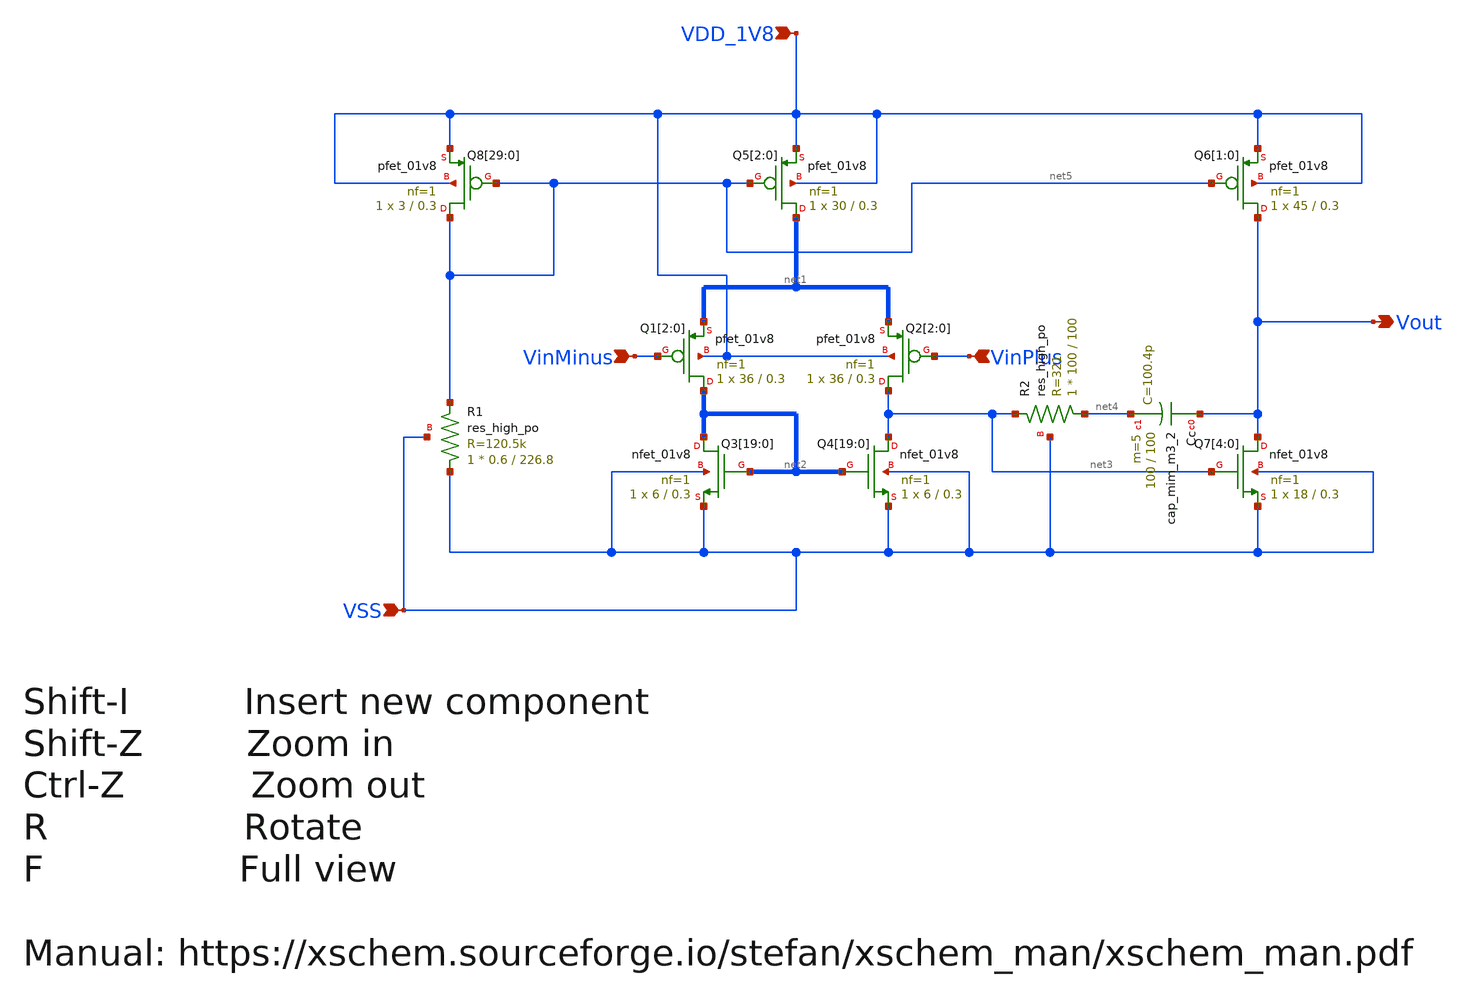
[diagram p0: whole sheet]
** sch_path: rply_mainopamp_sky130nm/design/RPLY_MAINOPAMP_SKY130NM/RPLY_MAINOPAMP.sch
**.subckt RPLY_MAINOPAMP Vout VinMinus VinPlus VDD_1V8 VSS
*.opin Vout
*.ipin VinMinus
*.ipin VinPlus
*.ipin VDD_1V8
*.ipin VSS
XQ8[29] net5 net5 VDD_1V8 VDD_1V8 sky130_fd_pr__pfet_01v8 L=0.3 W=3 nf=1 ad='int((nf+1)/2) * W/nf * 0.29'
+ as='int((nf+2)/2) * W/nf * 0.29' pd='2*int((nf+1)/2) * (W/nf + 0.29)' ps='2*int((nf+2)/2) * (W/nf + 0.29)'
+ nrd='0.29 / W' nrs='0.29 / W' sa=0 sb=0 sd=0 mult=1 m=1
XQ8[28] net5 net5 VDD_1V8 VDD_1V8 sky130_fd_pr__pfet_01v8 L=0.3 W=3 nf=1 ad='int((nf+1)/2) * W/nf * 0.29'
+ as='int((nf+2)/2) * W/nf * 0.29' pd='2*int((nf+1)/2) * (W/nf + 0.29)' ps='2*int((nf+2)/2) * (W/nf + 0.29)'
+ nrd='0.29 / W' nrs='0.29 / W' sa=0 sb=0 sd=0 mult=1 m=1
XQ8[27] net5 net5 VDD_1V8 VDD_1V8 sky130_fd_pr__pfet_01v8 L=0.3 W=3 nf=1 ad='int((nf+1)/2) * W/nf * 0.29'
+ as='int((nf+2)/2) * W/nf * 0.29' pd='2*int((nf+1)/2) * (W/nf + 0.29)' ps='2*int((nf+2)/2) * (W/nf + 0.29)'
+ nrd='0.29 / W' nrs='0.29 / W' sa=0 sb=0 sd=0 mult=1 m=1
XQ8[26] net5 net5 VDD_1V8 VDD_1V8 sky130_fd_pr__pfet_01v8 L=0.3 W=3 nf=1 ad='int((nf+1)/2) * W/nf * 0.29'
+ as='int((nf+2)/2) * W/nf * 0.29' pd='2*int((nf+1)/2) * (W/nf + 0.29)' ps='2*int((nf+2)/2) * (W/nf + 0.29)'
+ nrd='0.29 / W' nrs='0.29 / W' sa=0 sb=0 sd=0 mult=1 m=1
XQ8[25] net5 net5 VDD_1V8 VDD_1V8 sky130_fd_pr__pfet_01v8 L=0.3 W=3 nf=1 ad='int((nf+1)/2) * W/nf * 0.29'
+ as='int((nf+2)/2) * W/nf * 0.29' pd='2*int((nf+1)/2) * (W/nf + 0.29)' ps='2*int((nf+2)/2) * (W/nf + 0.29)'
+ nrd='0.29 / W' nrs='0.29 / W' sa=0 sb=0 sd=0 mult=1 m=1
XQ8[24] net5 net5 VDD_1V8 VDD_1V8 sky130_fd_pr__pfet_01v8 L=0.3 W=3 nf=1 ad='int((nf+1)/2) * W/nf * 0.29'
+ as='int((nf+2)/2) * W/nf * 0.29' pd='2*int((nf+1)/2) * (W/nf + 0.29)' ps='2*int((nf+2)/2) * (W/nf + 0.29)'
+ nrd='0.29 / W' nrs='0.29 / W' sa=0 sb=0 sd=0 mult=1 m=1
XQ8[23] net5 net5 VDD_1V8 VDD_1V8 sky130_fd_pr__pfet_01v8 L=0.3 W=3 nf=1 ad='int((nf+1)/2) * W/nf * 0.29'
+ as='int((nf+2)/2) * W/nf * 0.29' pd='2*int((nf+1)/2) * (W/nf + 0.29)' ps='2*int((nf+2)/2) * (W/nf + 0.29)'
+ nrd='0.29 / W' nrs='0.29 / W' sa=0 sb=0 sd=0 mult=1 m=1
XQ8[22] net5 net5 VDD_1V8 VDD_1V8 sky130_fd_pr__pfet_01v8 L=0.3 W=3 nf=1 ad='int((nf+1)/2) * W/nf * 0.29'
+ as='int((nf+2)/2) * W/nf * 0.29' pd='2*int((nf+1)/2) * (W/nf + 0.29)' ps='2*int((nf+2)/2) * (W/nf + 0.29)'
+ nrd='0.29 / W' nrs='0.29 / W' sa=0 sb=0 sd=0 mult=1 m=1
XQ8[21] net5 net5 VDD_1V8 VDD_1V8 sky130_fd_pr__pfet_01v8 L=0.3 W=3 nf=1 ad='int((nf+1)/2) * W/nf * 0.29'
+ as='int((nf+2)/2) * W/nf * 0.29' pd='2*int((nf+1)/2) * (W/nf + 0.29)' ps='2*int((nf+2)/2) * (W/nf + 0.29)'
+ nrd='0.29 / W' nrs='0.29 / W' sa=0 sb=0 sd=0 mult=1 m=1
XQ8[20] net5 net5 VDD_1V8 VDD_1V8 sky130_fd_pr__pfet_01v8 L=0.3 W=3 nf=1 ad='int((nf+1)/2) * W/nf * 0.29'
+ as='int((nf+2)/2) * W/nf * 0.29' pd='2*int((nf+1)/2) * (W/nf + 0.29)' ps='2*int((nf+2)/2) * (W/nf + 0.29)'
+ nrd='0.29 / W' nrs='0.29 / W' sa=0 sb=0 sd=0 mult=1 m=1
XQ8[19] net5 net5 VDD_1V8 VDD_1V8 sky130_fd_pr__pfet_01v8 L=0.3 W=3 nf=1 ad='int((nf+1)/2) * W/nf * 0.29'
+ as='int((nf+2)/2) * W/nf * 0.29' pd='2*int((nf+1)/2) * (W/nf + 0.29)' ps='2*int((nf+2)/2) * (W/nf + 0.29)'
+ nrd='0.29 / W' nrs='0.29 / W' sa=0 sb=0 sd=0 mult=1 m=1
XQ8[18] net5 net5 VDD_1V8 VDD_1V8 sky130_fd_pr__pfet_01v8 L=0.3 W=3 nf=1 ad='int((nf+1)/2) * W/nf * 0.29'
+ as='int((nf+2)/2) * W/nf * 0.29' pd='2*int((nf+1)/2) * (W/nf + 0.29)' ps='2*int((nf+2)/2) * (W/nf + 0.29)'
+ nrd='0.29 / W' nrs='0.29 / W' sa=0 sb=0 sd=0 mult=1 m=1
XQ8[17] net5 net5 VDD_1V8 VDD_1V8 sky130_fd_pr__pfet_01v8 L=0.3 W=3 nf=1 ad='int((nf+1)/2) * W/nf * 0.29'
+ as='int((nf+2)/2) * W/nf * 0.29' pd='2*int((nf+1)/2) * (W/nf + 0.29)' ps='2*int((nf+2)/2) * (W/nf + 0.29)'
+ nrd='0.29 / W' nrs='0.29 / W' sa=0 sb=0 sd=0 mult=1 m=1
XQ8[16] net5 net5 VDD_1V8 VDD_1V8 sky130_fd_pr__pfet_01v8 L=0.3 W=3 nf=1 ad='int((nf+1)/2) * W/nf * 0.29'
+ as='int((nf+2)/2) * W/nf * 0.29' pd='2*int((nf+1)/2) * (W/nf + 0.29)' ps='2*int((nf+2)/2) * (W/nf + 0.29)'
+ nrd='0.29 / W' nrs='0.29 / W' sa=0 sb=0 sd=0 mult=1 m=1
XQ8[15] net5 net5 VDD_1V8 VDD_1V8 sky130_fd_pr__pfet_01v8 L=0.3 W=3 nf=1 ad='int((nf+1)/2) * W/nf * 0.29'
+ as='int((nf+2)/2) * W/nf * 0.29' pd='2*int((nf+1)/2) * (W/nf + 0.29)' ps='2*int((nf+2)/2) * (W/nf + 0.29)'
+ nrd='0.29 / W' nrs='0.29 / W' sa=0 sb=0 sd=0 mult=1 m=1
XQ8[14] net5 net5 VDD_1V8 VDD_1V8 sky130_fd_pr__pfet_01v8 L=0.3 W=3 nf=1 ad='int((nf+1)/2) * W/nf * 0.29'
+ as='int((nf+2)/2) * W/nf * 0.29' pd='2*int((nf+1)/2) * (W/nf + 0.29)' ps='2*int((nf+2)/2) * (W/nf + 0.29)'
+ nrd='0.29 / W' nrs='0.29 / W' sa=0 sb=0 sd=0 mult=1 m=1
XQ8[13] net5 net5 VDD_1V8 VDD_1V8 sky130_fd_pr__pfet_01v8 L=0.3 W=3 nf=1 ad='int((nf+1)/2) * W/nf * 0.29'
+ as='int((nf+2)/2) * W/nf * 0.29' pd='2*int((nf+1)/2) * (W/nf + 0.29)' ps='2*int((nf+2)/2) * (W/nf + 0.29)'
+ nrd='0.29 / W' nrs='0.29 / W' sa=0 sb=0 sd=0 mult=1 m=1
XQ8[12] net5 net5 VDD_1V8 VDD_1V8 sky130_fd_pr__pfet_01v8 L=0.3 W=3 nf=1 ad='int((nf+1)/2) * W/nf * 0.29'
+ as='int((nf+2)/2) * W/nf * 0.29' pd='2*int((nf+1)/2) * (W/nf + 0.29)' ps='2*int((nf+2)/2) * (W/nf + 0.29)'
+ nrd='0.29 / W' nrs='0.29 / W' sa=0 sb=0 sd=0 mult=1 m=1
XQ8[11] net5 net5 VDD_1V8 VDD_1V8 sky130_fd_pr__pfet_01v8 L=0.3 W=3 nf=1 ad='int((nf+1)/2) * W/nf * 0.29'
+ as='int((nf+2)/2) * W/nf * 0.29' pd='2*int((nf+1)/2) * (W/nf + 0.29)' ps='2*int((nf+2)/2) * (W/nf + 0.29)'
+ nrd='0.29 / W' nrs='0.29 / W' sa=0 sb=0 sd=0 mult=1 m=1
XQ8[10] net5 net5 VDD_1V8 VDD_1V8 sky130_fd_pr__pfet_01v8 L=0.3 W=3 nf=1 ad='int((nf+1)/2) * W/nf * 0.29'
+ as='int((nf+2)/2) * W/nf * 0.29' pd='2*int((nf+1)/2) * (W/nf + 0.29)' ps='2*int((nf+2)/2) * (W/nf + 0.29)'
+ nrd='0.29 / W' nrs='0.29 / W' sa=0 sb=0 sd=0 mult=1 m=1
XQ8[9] net5 net5 VDD_1V8 VDD_1V8 sky130_fd_pr__pfet_01v8 L=0.3 W=3 nf=1 ad='int((nf+1)/2) * W/nf * 0.29'
+ as='int((nf+2)/2) * W/nf * 0.29' pd='2*int((nf+1)/2) * (W/nf + 0.29)' ps='2*int((nf+2)/2) * (W/nf + 0.29)'
+ nrd='0.29 / W' nrs='0.29 / W' sa=0 sb=0 sd=0 mult=1 m=1
XQ8[8] net5 net5 VDD_1V8 VDD_1V8 sky130_fd_pr__pfet_01v8 L=0.3 W=3 nf=1 ad='int((nf+1)/2) * W/nf * 0.29'
+ as='int((nf+2)/2) * W/nf * 0.29' pd='2*int((nf+1)/2) * (W/nf + 0.29)' ps='2*int((nf+2)/2) * (W/nf + 0.29)'
+ nrd='0.29 / W' nrs='0.29 / W' sa=0 sb=0 sd=0 mult=1 m=1
XQ8[7] net5 net5 VDD_1V8 VDD_1V8 sky130_fd_pr__pfet_01v8 L=0.3 W=3 nf=1 ad='int((nf+1)/2) * W/nf * 0.29'
+ as='int((nf+2)/2) * W/nf * 0.29' pd='2*int((nf+1)/2) * (W/nf + 0.29)' ps='2*int((nf+2)/2) * (W/nf + 0.29)'
+ nrd='0.29 / W' nrs='0.29 / W' sa=0 sb=0 sd=0 mult=1 m=1
XQ8[6] net5 net5 VDD_1V8 VDD_1V8 sky130_fd_pr__pfet_01v8 L=0.3 W=3 nf=1 ad='int((nf+1)/2) * W/nf * 0.29'
+ as='int((nf+2)/2) * W/nf * 0.29' pd='2*int((nf+1)/2) * (W/nf + 0.29)' ps='2*int((nf+2)/2) * (W/nf + 0.29)'
+ nrd='0.29 / W' nrs='0.29 / W' sa=0 sb=0 sd=0 mult=1 m=1
XQ8[5] net5 net5 VDD_1V8 VDD_1V8 sky130_fd_pr__pfet_01v8 L=0.3 W=3 nf=1 ad='int((nf+1)/2) * W/nf * 0.29'
+ as='int((nf+2)/2) * W/nf * 0.29' pd='2*int((nf+1)/2) * (W/nf + 0.29)' ps='2*int((nf+2)/2) * (W/nf + 0.29)'
+ nrd='0.29 / W' nrs='0.29 / W' sa=0 sb=0 sd=0 mult=1 m=1
XQ8[4] net5 net5 VDD_1V8 VDD_1V8 sky130_fd_pr__pfet_01v8 L=0.3 W=3 nf=1 ad='int((nf+1)/2) * W/nf * 0.29'
+ as='int((nf+2)/2) * W/nf * 0.29' pd='2*int((nf+1)/2) * (W/nf + 0.29)' ps='2*int((nf+2)/2) * (W/nf + 0.29)'
+ nrd='0.29 / W' nrs='0.29 / W' sa=0 sb=0 sd=0 mult=1 m=1
XQ8[3] net5 net5 VDD_1V8 VDD_1V8 sky130_fd_pr__pfet_01v8 L=0.3 W=3 nf=1 ad='int((nf+1)/2) * W/nf * 0.29'
+ as='int((nf+2)/2) * W/nf * 0.29' pd='2*int((nf+1)/2) * (W/nf + 0.29)' ps='2*int((nf+2)/2) * (W/nf + 0.29)'
+ nrd='0.29 / W' nrs='0.29 / W' sa=0 sb=0 sd=0 mult=1 m=1
XQ8[2] net5 net5 VDD_1V8 VDD_1V8 sky130_fd_pr__pfet_01v8 L=0.3 W=3 nf=1 ad='int((nf+1)/2) * W/nf * 0.29'
+ as='int((nf+2)/2) * W/nf * 0.29' pd='2*int((nf+1)/2) * (W/nf + 0.29)' ps='2*int((nf+2)/2) * (W/nf + 0.29)'
+ nrd='0.29 / W' nrs='0.29 / W' sa=0 sb=0 sd=0 mult=1 m=1
XQ8[1] net5 net5 VDD_1V8 VDD_1V8 sky130_fd_pr__pfet_01v8 L=0.3 W=3 nf=1 ad='int((nf+1)/2) * W/nf * 0.29'
+ as='int((nf+2)/2) * W/nf * 0.29' pd='2*int((nf+1)/2) * (W/nf + 0.29)' ps='2*int((nf+2)/2) * (W/nf + 0.29)'
+ nrd='0.29 / W' nrs='0.29 / W' sa=0 sb=0 sd=0 mult=1 m=1
XQ8[0] net5 net5 VDD_1V8 VDD_1V8 sky130_fd_pr__pfet_01v8 L=0.3 W=3 nf=1 ad='int((nf+1)/2) * W/nf * 0.29'
+ as='int((nf+2)/2) * W/nf * 0.29' pd='2*int((nf+1)/2) * (W/nf + 0.29)' ps='2*int((nf+2)/2) * (W/nf + 0.29)'
+ nrd='0.29 / W' nrs='0.29 / W' sa=0 sb=0 sd=0 mult=1 m=1
XQ5[2] net1[2] net5 VDD_1V8 VDD_1V8 sky130_fd_pr__pfet_01v8 L=0.3 W=30 nf=1 ad='int((nf+1)/2) * W/nf * 0.29'
+ as='int((nf+2)/2) * W/nf * 0.29' pd='2*int((nf+1)/2) * (W/nf + 0.29)' ps='2*int((nf+2)/2) * (W/nf + 0.29)'
+ nrd='0.29 / W' nrs='0.29 / W' sa=0 sb=0 sd=0 mult=1 m=1
XQ5[1] net1[1] net5 VDD_1V8 VDD_1V8 sky130_fd_pr__pfet_01v8 L=0.3 W=30 nf=1 ad='int((nf+1)/2) * W/nf * 0.29'
+ as='int((nf+2)/2) * W/nf * 0.29' pd='2*int((nf+1)/2) * (W/nf + 0.29)' ps='2*int((nf+2)/2) * (W/nf + 0.29)'
+ nrd='0.29 / W' nrs='0.29 / W' sa=0 sb=0 sd=0 mult=1 m=1
XQ5[0] net1[0] net5 VDD_1V8 VDD_1V8 sky130_fd_pr__pfet_01v8 L=0.3 W=30 nf=1 ad='int((nf+1)/2) * W/nf * 0.29'
+ as='int((nf+2)/2) * W/nf * 0.29' pd='2*int((nf+1)/2) * (W/nf + 0.29)' ps='2*int((nf+2)/2) * (W/nf + 0.29)'
+ nrd='0.29 / W' nrs='0.29 / W' sa=0 sb=0 sd=0 mult=1 m=1
XQ6[1] Vout net5 VDD_1V8 VDD_1V8 sky130_fd_pr__pfet_01v8 L=0.3 W=45 nf=1 ad='int((nf+1)/2) * W/nf * 0.29'
+ as='int((nf+2)/2) * W/nf * 0.29' pd='2*int((nf+1)/2) * (W/nf + 0.29)' ps='2*int((nf+2)/2) * (W/nf + 0.29)'
+ nrd='0.29 / W' nrs='0.29 / W' sa=0 sb=0 sd=0 mult=1 m=1
XQ6[0] Vout net5 VDD_1V8 VDD_1V8 sky130_fd_pr__pfet_01v8 L=0.3 W=45 nf=1 ad='int((nf+1)/2) * W/nf * 0.29'
+ as='int((nf+2)/2) * W/nf * 0.29' pd='2*int((nf+1)/2) * (W/nf + 0.29)' ps='2*int((nf+2)/2) * (W/nf + 0.29)'
+ nrd='0.29 / W' nrs='0.29 / W' sa=0 sb=0 sd=0 mult=1 m=1
XQ1[2] net2[2] VinMinus net1[2] VDD_1V8 sky130_fd_pr__pfet_01v8 L=0.3 W=36 nf=1 ad='int((nf+1)/2) * W/nf * 0.29'
+ as='int((nf+2)/2) * W/nf * 0.29' pd='2*int((nf+1)/2) * (W/nf + 0.29)' ps='2*int((nf+2)/2) * (W/nf + 0.29)'
+ nrd='0.29 / W' nrs='0.29 / W' sa=0 sb=0 sd=0 mult=1 m=1
XQ1[1] net2[1] VinMinus net1[1] VDD_1V8 sky130_fd_pr__pfet_01v8 L=0.3 W=36 nf=1 ad='int((nf+1)/2) * W/nf * 0.29'
+ as='int((nf+2)/2) * W/nf * 0.29' pd='2*int((nf+1)/2) * (W/nf + 0.29)' ps='2*int((nf+2)/2) * (W/nf + 0.29)'
+ nrd='0.29 / W' nrs='0.29 / W' sa=0 sb=0 sd=0 mult=1 m=1
XQ1[0] net2[0] VinMinus net1[0] VDD_1V8 sky130_fd_pr__pfet_01v8 L=0.3 W=36 nf=1 ad='int((nf+1)/2) * W/nf * 0.29'
+ as='int((nf+2)/2) * W/nf * 0.29' pd='2*int((nf+1)/2) * (W/nf + 0.29)' ps='2*int((nf+2)/2) * (W/nf + 0.29)'
+ nrd='0.29 / W' nrs='0.29 / W' sa=0 sb=0 sd=0 mult=1 m=1
XQ2[2] net3 VinPlus net1[2] VDD_1V8 sky130_fd_pr__pfet_01v8 L=0.3 W=36 nf=1 ad='int((nf+1)/2) * W/nf * 0.29'
+ as='int((nf+2)/2) * W/nf * 0.29' pd='2*int((nf+1)/2) * (W/nf + 0.29)' ps='2*int((nf+2)/2) * (W/nf + 0.29)'
+ nrd='0.29 / W' nrs='0.29 / W' sa=0 sb=0 sd=0 mult=1 m=1
XQ2[1] net3 VinPlus net1[1] VDD_1V8 sky130_fd_pr__pfet_01v8 L=0.3 W=36 nf=1 ad='int((nf+1)/2) * W/nf * 0.29'
+ as='int((nf+2)/2) * W/nf * 0.29' pd='2*int((nf+1)/2) * (W/nf + 0.29)' ps='2*int((nf+2)/2) * (W/nf + 0.29)'
+ nrd='0.29 / W' nrs='0.29 / W' sa=0 sb=0 sd=0 mult=1 m=1
XQ2[0] net3 VinPlus net1[0] VDD_1V8 sky130_fd_pr__pfet_01v8 L=0.3 W=36 nf=1 ad='int((nf+1)/2) * W/nf * 0.29'
+ as='int((nf+2)/2) * W/nf * 0.29' pd='2*int((nf+1)/2) * (W/nf + 0.29)' ps='2*int((nf+2)/2) * (W/nf + 0.29)'
+ nrd='0.29 / W' nrs='0.29 / W' sa=0 sb=0 sd=0 mult=1 m=1
XQ4[19] net3 net2[2] VSS VSS sky130_fd_pr__nfet_01v8 L=0.3 W=6 nf=1 ad='int((nf+1)/2) * W/nf * 0.29'
+ as='int((nf+2)/2) * W/nf * 0.29' pd='2*int((nf+1)/2) * (W/nf + 0.29)' ps='2*int((nf+2)/2) * (W/nf + 0.29)'
+ nrd='0.29 / W' nrs='0.29 / W' sa=0 sb=0 sd=0 mult=1 m=1
XQ4[18] net3 net2[1] VSS VSS sky130_fd_pr__nfet_01v8 L=0.3 W=6 nf=1 ad='int((nf+1)/2) * W/nf * 0.29'
+ as='int((nf+2)/2) * W/nf * 0.29' pd='2*int((nf+1)/2) * (W/nf + 0.29)' ps='2*int((nf+2)/2) * (W/nf + 0.29)'
+ nrd='0.29 / W' nrs='0.29 / W' sa=0 sb=0 sd=0 mult=1 m=1
XQ4[17] net3 net2[0] VSS VSS sky130_fd_pr__nfet_01v8 L=0.3 W=6 nf=1 ad='int((nf+1)/2) * W/nf * 0.29'
+ as='int((nf+2)/2) * W/nf * 0.29' pd='2*int((nf+1)/2) * (W/nf + 0.29)' ps='2*int((nf+2)/2) * (W/nf + 0.29)'
+ nrd='0.29 / W' nrs='0.29 / W' sa=0 sb=0 sd=0 mult=1 m=1
XQ4[16] net3 net2[2] VSS VSS sky130_fd_pr__nfet_01v8 L=0.3 W=6 nf=1 ad='int((nf+1)/2) * W/nf * 0.29'
+ as='int((nf+2)/2) * W/nf * 0.29' pd='2*int((nf+1)/2) * (W/nf + 0.29)' ps='2*int((nf+2)/2) * (W/nf + 0.29)'
+ nrd='0.29 / W' nrs='0.29 / W' sa=0 sb=0 sd=0 mult=1 m=1
XQ4[15] net3 net2[1] VSS VSS sky130_fd_pr__nfet_01v8 L=0.3 W=6 nf=1 ad='int((nf+1)/2) * W/nf * 0.29'
+ as='int((nf+2)/2) * W/nf * 0.29' pd='2*int((nf+1)/2) * (W/nf + 0.29)' ps='2*int((nf+2)/2) * (W/nf + 0.29)'
+ nrd='0.29 / W' nrs='0.29 / W' sa=0 sb=0 sd=0 mult=1 m=1
XQ4[14] net3 net2[0] VSS VSS sky130_fd_pr__nfet_01v8 L=0.3 W=6 nf=1 ad='int((nf+1)/2) * W/nf * 0.29'
+ as='int((nf+2)/2) * W/nf * 0.29' pd='2*int((nf+1)/2) * (W/nf + 0.29)' ps='2*int((nf+2)/2) * (W/nf + 0.29)'
+ nrd='0.29 / W' nrs='0.29 / W' sa=0 sb=0 sd=0 mult=1 m=1
XQ4[13] net3 net2[2] VSS VSS sky130_fd_pr__nfet_01v8 L=0.3 W=6 nf=1 ad='int((nf+1)/2) * W/nf * 0.29'
+ as='int((nf+2)/2) * W/nf * 0.29' pd='2*int((nf+1)/2) * (W/nf + 0.29)' ps='2*int((nf+2)/2) * (W/nf + 0.29)'
+ nrd='0.29 / W' nrs='0.29 / W' sa=0 sb=0 sd=0 mult=1 m=1
XQ4[12] net3 net2[1] VSS VSS sky130_fd_pr__nfet_01v8 L=0.3 W=6 nf=1 ad='int((nf+1)/2) * W/nf * 0.29'
+ as='int((nf+2)/2) * W/nf * 0.29' pd='2*int((nf+1)/2) * (W/nf + 0.29)' ps='2*int((nf+2)/2) * (W/nf + 0.29)'
+ nrd='0.29 / W' nrs='0.29 / W' sa=0 sb=0 sd=0 mult=1 m=1
XQ4[11] net3 net2[0] VSS VSS sky130_fd_pr__nfet_01v8 L=0.3 W=6 nf=1 ad='int((nf+1)/2) * W/nf * 0.29'
+ as='int((nf+2)/2) * W/nf * 0.29' pd='2*int((nf+1)/2) * (W/nf + 0.29)' ps='2*int((nf+2)/2) * (W/nf + 0.29)'
+ nrd='0.29 / W' nrs='0.29 / W' sa=0 sb=0 sd=0 mult=1 m=1
XQ4[10] net3 net2[2] VSS VSS sky130_fd_pr__nfet_01v8 L=0.3 W=6 nf=1 ad='int((nf+1)/2) * W/nf * 0.29'
+ as='int((nf+2)/2) * W/nf * 0.29' pd='2*int((nf+1)/2) * (W/nf + 0.29)' ps='2*int((nf+2)/2) * (W/nf + 0.29)'
+ nrd='0.29 / W' nrs='0.29 / W' sa=0 sb=0 sd=0 mult=1 m=1
XQ4[9] net3 net2[1] VSS VSS sky130_fd_pr__nfet_01v8 L=0.3 W=6 nf=1 ad='int((nf+1)/2) * W/nf * 0.29' as='int((nf+2)/2) * W/nf * 0.29'
+ pd='2*int((nf+1)/2) * (W/nf + 0.29)' ps='2*int((nf+2)/2) * (W/nf + 0.29)' nrd='0.29 / W' nrs='0.29 / W'
+ sa=0 sb=0 sd=0 mult=1 m=1
XQ4[8] net3 net2[0] VSS VSS sky130_fd_pr__nfet_01v8 L=0.3 W=6 nf=1 ad='int((nf+1)/2) * W/nf * 0.29' as='int((nf+2)/2) * W/nf * 0.29'
+ pd='2*int((nf+1)/2) * (W/nf + 0.29)' ps='2*int((nf+2)/2) * (W/nf + 0.29)' nrd='0.29 / W' nrs='0.29 / W'
+ sa=0 sb=0 sd=0 mult=1 m=1
XQ4[7] net3 net2[2] VSS VSS sky130_fd_pr__nfet_01v8 L=0.3 W=6 nf=1 ad='int((nf+1)/2) * W/nf * 0.29' as='int((nf+2)/2) * W/nf * 0.29'
+ pd='2*int((nf+1)/2) * (W/nf + 0.29)' ps='2*int((nf+2)/2) * (W/nf + 0.29)' nrd='0.29 / W' nrs='0.29 / W'
+ sa=0 sb=0 sd=0 mult=1 m=1
XQ4[6] net3 net2[1] VSS VSS sky130_fd_pr__nfet_01v8 L=0.3 W=6 nf=1 ad='int((nf+1)/2) * W/nf * 0.29' as='int((nf+2)/2) * W/nf * 0.29'
+ pd='2*int((nf+1)/2) * (W/nf + 0.29)' ps='2*int((nf+2)/2) * (W/nf + 0.29)' nrd='0.29 / W' nrs='0.29 / W'
+ sa=0 sb=0 sd=0 mult=1 m=1
XQ4[5] net3 net2[0] VSS VSS sky130_fd_pr__nfet_01v8 L=0.3 W=6 nf=1 ad='int((nf+1)/2) * W/nf * 0.29' as='int((nf+2)/2) * W/nf * 0.29'
+ pd='2*int((nf+1)/2) * (W/nf + 0.29)' ps='2*int((nf+2)/2) * (W/nf + 0.29)' nrd='0.29 / W' nrs='0.29 / W'
+ sa=0 sb=0 sd=0 mult=1 m=1
XQ4[4] net3 net2[2] VSS VSS sky130_fd_pr__nfet_01v8 L=0.3 W=6 nf=1 ad='int((nf+1)/2) * W/nf * 0.29' as='int((nf+2)/2) * W/nf * 0.29'
+ pd='2*int((nf+1)/2) * (W/nf + 0.29)' ps='2*int((nf+2)/2) * (W/nf + 0.29)' nrd='0.29 / W' nrs='0.29 / W'
+ sa=0 sb=0 sd=0 mult=1 m=1
XQ4[3] net3 net2[1] VSS VSS sky130_fd_pr__nfet_01v8 L=0.3 W=6 nf=1 ad='int((nf+1)/2) * W/nf * 0.29' as='int((nf+2)/2) * W/nf * 0.29'
+ pd='2*int((nf+1)/2) * (W/nf + 0.29)' ps='2*int((nf+2)/2) * (W/nf + 0.29)' nrd='0.29 / W' nrs='0.29 / W'
+ sa=0 sb=0 sd=0 mult=1 m=1
XQ4[2] net3 net2[0] VSS VSS sky130_fd_pr__nfet_01v8 L=0.3 W=6 nf=1 ad='int((nf+1)/2) * W/nf * 0.29' as='int((nf+2)/2) * W/nf * 0.29'
+ pd='2*int((nf+1)/2) * (W/nf + 0.29)' ps='2*int((nf+2)/2) * (W/nf + 0.29)' nrd='0.29 / W' nrs='0.29 / W'
+ sa=0 sb=0 sd=0 mult=1 m=1
XQ4[1] net3 net2[2] VSS VSS sky130_fd_pr__nfet_01v8 L=0.3 W=6 nf=1 ad='int((nf+1)/2) * W/nf * 0.29' as='int((nf+2)/2) * W/nf * 0.29'
+ pd='2*int((nf+1)/2) * (W/nf + 0.29)' ps='2*int((nf+2)/2) * (W/nf + 0.29)' nrd='0.29 / W' nrs='0.29 / W'
+ sa=0 sb=0 sd=0 mult=1 m=1
XQ4[0] net3 net2[1] VSS VSS sky130_fd_pr__nfet_01v8 L=0.3 W=6 nf=1 ad='int((nf+1)/2) * W/nf * 0.29' as='int((nf+2)/2) * W/nf * 0.29'
+ pd='2*int((nf+1)/2) * (W/nf + 0.29)' ps='2*int((nf+2)/2) * (W/nf + 0.29)' nrd='0.29 / W' nrs='0.29 / W'
+ sa=0 sb=0 sd=0 mult=1 m=1
XQ3[19] net2[2] net2[2] VSS VSS sky130_fd_pr__nfet_01v8 L=0.3 W=6 nf=1 ad='int((nf+1)/2) * W/nf * 0.29'
+ as='int((nf+2)/2) * W/nf * 0.29' pd='2*int((nf+1)/2) * (W/nf + 0.29)' ps='2*int((nf+2)/2) * (W/nf + 0.29)'
+ nrd='0.29 / W' nrs='0.29 / W' sa=0 sb=0 sd=0 mult=1 m=1
XQ3[18] net2[1] net2[1] VSS VSS sky130_fd_pr__nfet_01v8 L=0.3 W=6 nf=1 ad='int((nf+1)/2) * W/nf * 0.29'
+ as='int((nf+2)/2) * W/nf * 0.29' pd='2*int((nf+1)/2) * (W/nf + 0.29)' ps='2*int((nf+2)/2) * (W/nf + 0.29)'
+ nrd='0.29 / W' nrs='0.29 / W' sa=0 sb=0 sd=0 mult=1 m=1
XQ3[17] net2[0] net2[0] VSS VSS sky130_fd_pr__nfet_01v8 L=0.3 W=6 nf=1 ad='int((nf+1)/2) * W/nf * 0.29'
+ as='int((nf+2)/2) * W/nf * 0.29' pd='2*int((nf+1)/2) * (W/nf + 0.29)' ps='2*int((nf+2)/2) * (W/nf + 0.29)'
+ nrd='0.29 / W' nrs='0.29 / W' sa=0 sb=0 sd=0 mult=1 m=1
XQ3[16] net2[2] net2[2] VSS VSS sky130_fd_pr__nfet_01v8 L=0.3 W=6 nf=1 ad='int((nf+1)/2) * W/nf * 0.29'
+ as='int((nf+2)/2) * W/nf * 0.29' pd='2*int((nf+1)/2) * (W/nf + 0.29)' ps='2*int((nf+2)/2) * (W/nf + 0.29)'
+ nrd='0.29 / W' nrs='0.29 / W' sa=0 sb=0 sd=0 mult=1 m=1
XQ3[15] net2[1] net2[1] VSS VSS sky130_fd_pr__nfet_01v8 L=0.3 W=6 nf=1 ad='int((nf+1)/2) * W/nf * 0.29'
+ as='int((nf+2)/2) * W/nf * 0.29' pd='2*int((nf+1)/2) * (W/nf + 0.29)' ps='2*int((nf+2)/2) * (W/nf + 0.29)'
+ nrd='0.29 / W' nrs='0.29 / W' sa=0 sb=0 sd=0 mult=1 m=1
XQ3[14] net2[0] net2[0] VSS VSS sky130_fd_pr__nfet_01v8 L=0.3 W=6 nf=1 ad='int((nf+1)/2) * W/nf * 0.29'
+ as='int((nf+2)/2) * W/nf * 0.29' pd='2*int((nf+1)/2) * (W/nf + 0.29)' ps='2*int((nf+2)/2) * (W/nf + 0.29)'
+ nrd='0.29 / W' nrs='0.29 / W' sa=0 sb=0 sd=0 mult=1 m=1
XQ3[13] net2[2] net2[2] VSS VSS sky130_fd_pr__nfet_01v8 L=0.3 W=6 nf=1 ad='int((nf+1)/2) * W/nf * 0.29'
+ as='int((nf+2)/2) * W/nf * 0.29' pd='2*int((nf+1)/2) * (W/nf + 0.29)' ps='2*int((nf+2)/2) * (W/nf + 0.29)'
+ nrd='0.29 / W' nrs='0.29 / W' sa=0 sb=0 sd=0 mult=1 m=1
XQ3[12] net2[1] net2[1] VSS VSS sky130_fd_pr__nfet_01v8 L=0.3 W=6 nf=1 ad='int((nf+1)/2) * W/nf * 0.29'
+ as='int((nf+2)/2) * W/nf * 0.29' pd='2*int((nf+1)/2) * (W/nf + 0.29)' ps='2*int((nf+2)/2) * (W/nf + 0.29)'
+ nrd='0.29 / W' nrs='0.29 / W' sa=0 sb=0 sd=0 mult=1 m=1
XQ3[11] net2[0] net2[0] VSS VSS sky130_fd_pr__nfet_01v8 L=0.3 W=6 nf=1 ad='int((nf+1)/2) * W/nf * 0.29'
+ as='int((nf+2)/2) * W/nf * 0.29' pd='2*int((nf+1)/2) * (W/nf + 0.29)' ps='2*int((nf+2)/2) * (W/nf + 0.29)'
+ nrd='0.29 / W' nrs='0.29 / W' sa=0 sb=0 sd=0 mult=1 m=1
XQ3[10] net2[2] net2[2] VSS VSS sky130_fd_pr__nfet_01v8 L=0.3 W=6 nf=1 ad='int((nf+1)/2) * W/nf * 0.29'
+ as='int((nf+2)/2) * W/nf * 0.29' pd='2*int((nf+1)/2) * (W/nf + 0.29)' ps='2*int((nf+2)/2) * (W/nf + 0.29)'
+ nrd='0.29 / W' nrs='0.29 / W' sa=0 sb=0 sd=0 mult=1 m=1
XQ3[9] net2[1] net2[1] VSS VSS sky130_fd_pr__nfet_01v8 L=0.3 W=6 nf=1 ad='int((nf+1)/2) * W/nf * 0.29'
+ as='int((nf+2)/2) * W/nf * 0.29' pd='2*int((nf+1)/2) * (W/nf + 0.29)' ps='2*int((nf+2)/2) * (W/nf + 0.29)'
+ nrd='0.29 / W' nrs='0.29 / W' sa=0 sb=0 sd=0 mult=1 m=1
XQ3[8] net2[0] net2[0] VSS VSS sky130_fd_pr__nfet_01v8 L=0.3 W=6 nf=1 ad='int((nf+1)/2) * W/nf * 0.29'
+ as='int((nf+2)/2) * W/nf * 0.29' pd='2*int((nf+1)/2) * (W/nf + 0.29)' ps='2*int((nf+2)/2) * (W/nf + 0.29)'
+ nrd='0.29 / W' nrs='0.29 / W' sa=0 sb=0 sd=0 mult=1 m=1
XQ3[7] net2[2] net2[2] VSS VSS sky130_fd_pr__nfet_01v8 L=0.3 W=6 nf=1 ad='int((nf+1)/2) * W/nf * 0.29'
+ as='int((nf+2)/2) * W/nf * 0.29' pd='2*int((nf+1)/2) * (W/nf + 0.29)' ps='2*int((nf+2)/2) * (W/nf + 0.29)'
+ nrd='0.29 / W' nrs='0.29 / W' sa=0 sb=0 sd=0 mult=1 m=1
XQ3[6] net2[1] net2[1] VSS VSS sky130_fd_pr__nfet_01v8 L=0.3 W=6 nf=1 ad='int((nf+1)/2) * W/nf * 0.29'
+ as='int((nf+2)/2) * W/nf * 0.29' pd='2*int((nf+1)/2) * (W/nf + 0.29)' ps='2*int((nf+2)/2) * (W/nf + 0.29)'
+ nrd='0.29 / W' nrs='0.29 / W' sa=0 sb=0 sd=0 mult=1 m=1
XQ3[5] net2[0] net2[0] VSS VSS sky130_fd_pr__nfet_01v8 L=0.3 W=6 nf=1 ad='int((nf+1)/2) * W/nf * 0.29'
+ as='int((nf+2)/2) * W/nf * 0.29' pd='2*int((nf+1)/2) * (W/nf + 0.29)' ps='2*int((nf+2)/2) * (W/nf + 0.29)'
+ nrd='0.29 / W' nrs='0.29 / W' sa=0 sb=0 sd=0 mult=1 m=1
XQ3[4] net2[2] net2[2] VSS VSS sky130_fd_pr__nfet_01v8 L=0.3 W=6 nf=1 ad='int((nf+1)/2) * W/nf * 0.29'
+ as='int((nf+2)/2) * W/nf * 0.29' pd='2*int((nf+1)/2) * (W/nf + 0.29)' ps='2*int((nf+2)/2) * (W/nf + 0.29)'
+ nrd='0.29 / W' nrs='0.29 / W' sa=0 sb=0 sd=0 mult=1 m=1
XQ3[3] net2[1] net2[1] VSS VSS sky130_fd_pr__nfet_01v8 L=0.3 W=6 nf=1 ad='int((nf+1)/2) * W/nf * 0.29'
+ as='int((nf+2)/2) * W/nf * 0.29' pd='2*int((nf+1)/2) * (W/nf + 0.29)' ps='2*int((nf+2)/2) * (W/nf + 0.29)'
+ nrd='0.29 / W' nrs='0.29 / W' sa=0 sb=0 sd=0 mult=1 m=1
XQ3[2] net2[0] net2[0] VSS VSS sky130_fd_pr__nfet_01v8 L=0.3 W=6 nf=1 ad='int((nf+1)/2) * W/nf * 0.29'
+ as='int((nf+2)/2) * W/nf * 0.29' pd='2*int((nf+1)/2) * (W/nf + 0.29)' ps='2*int((nf+2)/2) * (W/nf + 0.29)'
+ nrd='0.29 / W' nrs='0.29 / W' sa=0 sb=0 sd=0 mult=1 m=1
XQ3[1] net2[2] net2[2] VSS VSS sky130_fd_pr__nfet_01v8 L=0.3 W=6 nf=1 ad='int((nf+1)/2) * W/nf * 0.29'
+ as='int((nf+2)/2) * W/nf * 0.29' pd='2*int((nf+1)/2) * (W/nf + 0.29)' ps='2*int((nf+2)/2) * (W/nf + 0.29)'
+ nrd='0.29 / W' nrs='0.29 / W' sa=0 sb=0 sd=0 mult=1 m=1
XQ3[0] net2[1] net2[1] VSS VSS sky130_fd_pr__nfet_01v8 L=0.3 W=6 nf=1 ad='int((nf+1)/2) * W/nf * 0.29'
+ as='int((nf+2)/2) * W/nf * 0.29' pd='2*int((nf+1)/2) * (W/nf + 0.29)' ps='2*int((nf+2)/2) * (W/nf + 0.29)'
+ nrd='0.29 / W' nrs='0.29 / W' sa=0 sb=0 sd=0 mult=1 m=1
XQ7[4] Vout net3 VSS VSS sky130_fd_pr__nfet_01v8 L=0.3 W=18 nf=1 ad='int((nf+1)/2) * W/nf * 0.29' as='int((nf+2)/2) * W/nf * 0.29'
+ pd='2*int((nf+1)/2) * (W/nf + 0.29)' ps='2*int((nf+2)/2) * (W/nf + 0.29)' nrd='0.29 / W' nrs='0.29 / W'
+ sa=0 sb=0 sd=0 mult=1 m=1
XQ7[3] Vout net3 VSS VSS sky130_fd_pr__nfet_01v8 L=0.3 W=18 nf=1 ad='int((nf+1)/2) * W/nf * 0.29' as='int((nf+2)/2) * W/nf * 0.29'
+ pd='2*int((nf+1)/2) * (W/nf + 0.29)' ps='2*int((nf+2)/2) * (W/nf + 0.29)' nrd='0.29 / W' nrs='0.29 / W'
+ sa=0 sb=0 sd=0 mult=1 m=1
XQ7[2] Vout net3 VSS VSS sky130_fd_pr__nfet_01v8 L=0.3 W=18 nf=1 ad='int((nf+1)/2) * W/nf * 0.29' as='int((nf+2)/2) * W/nf * 0.29'
+ pd='2*int((nf+1)/2) * (W/nf + 0.29)' ps='2*int((nf+2)/2) * (W/nf + 0.29)' nrd='0.29 / W' nrs='0.29 / W'
+ sa=0 sb=0 sd=0 mult=1 m=1
XQ7[1] Vout net3 VSS VSS sky130_fd_pr__nfet_01v8 L=0.3 W=18 nf=1 ad='int((nf+1)/2) * W/nf * 0.29' as='int((nf+2)/2) * W/nf * 0.29'
+ pd='2*int((nf+1)/2) * (W/nf + 0.29)' ps='2*int((nf+2)/2) * (W/nf + 0.29)' nrd='0.29 / W' nrs='0.29 / W'
+ sa=0 sb=0 sd=0 mult=1 m=1
XQ7[0] Vout net3 VSS VSS sky130_fd_pr__nfet_01v8 L=0.3 W=18 nf=1 ad='int((nf+1)/2) * W/nf * 0.29' as='int((nf+2)/2) * W/nf * 0.29'
+ pd='2*int((nf+1)/2) * (W/nf + 0.29)' ps='2*int((nf+2)/2) * (W/nf + 0.29)' nrd='0.29 / W' nrs='0.29 / W'
+ sa=0 sb=0 sd=0 mult=1 m=1
XCc Vout net4 sky130_fd_pr__cap_mim_m3_2 W=100 L=100 MF=5 m=5
XR1 VSS net5 VSS sky130_fd_pr__res_high_po W=0.6 L=226.8 mult=1 m=1
XR2 net4 net3 VSS sky130_fd_pr__res_high_po W=100 L=100 mult=1 m=1
**.ends
.end
